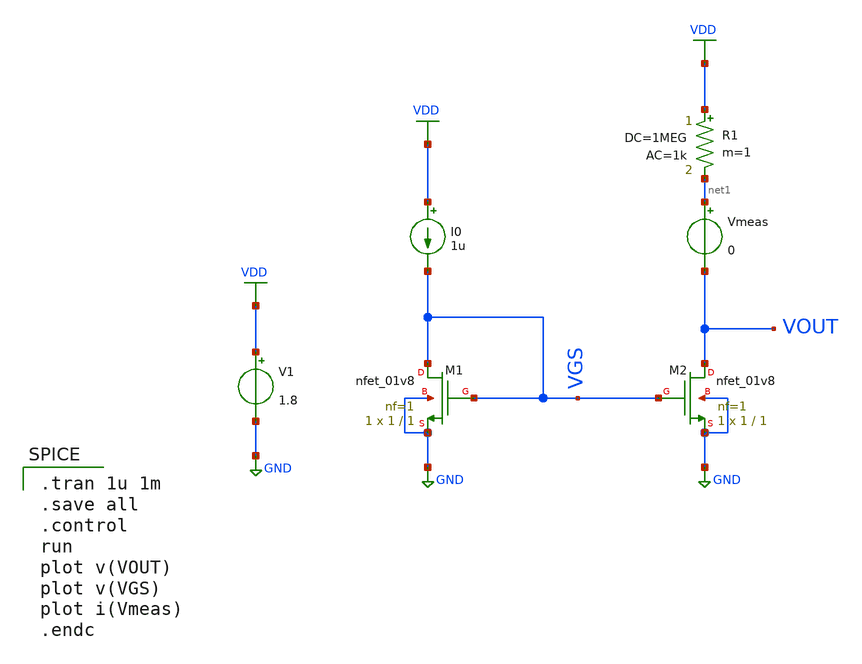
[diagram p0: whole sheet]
** sch_path: Circuits/Examples/Analog/Current_mirror/Basic_CURRMIRR.sch
**.subckt Basic_CURRMIRR
V1 VDD GND 1.8
XM1 VGS VGS GND GND sky130_fd_pr__nfet_01v8 L=1 W=1 nf=1 ad='int((nf+1)/2) * W/nf * 0.29' as='int((nf+2)/2) * W/nf * 0.29'
+ pd='2*int((nf+1)/2) * (W/nf + 0.29)' ps='2*int((nf+2)/2) * (W/nf + 0.29)' nrd='0.29 / W' nrs='0.29 / W'
+ sa=0 sb=0 sd=0 mult=1 m=1
I0 VDD VGS 1u
R1 VDD net1 1MEG ac=1k m=1
XM2 VOUT VGS GND GND sky130_fd_pr__nfet_01v8 L=1 W=1 nf=1 ad='int((nf+1)/2) * W/nf * 0.29' as='int((nf+2)/2) * W/nf * 0.29'
+ pd='2*int((nf+1)/2) * (W/nf + 0.29)' ps='2*int((nf+2)/2) * (W/nf + 0.29)' nrd='0.29 / W' nrs='0.29 / W'
+ sa=0 sb=0 sd=0 mult=1 m=1
Vmeas net1 VOUT 0
**** begin user architecture code
 ** manual skywater pdks install (with patches applied)
* .lib $::SKYWATER_MODELS/models/sky130.lib.spice tt

** opencircuitdesign pdks install
.lib $::SKYWATER_MODELS/sky130.lib.spice tt

.param mc_mm_switch=0
.param mc_pr_switch=0


.tran 1u 1m
.save all
.control
run
plot v(VOUT)
plot v(VGS)
plot i(Vmeas)
.endc


**** end user architecture code
**.ends
.GLOBAL GND
.GLOBAL VDD
.end
